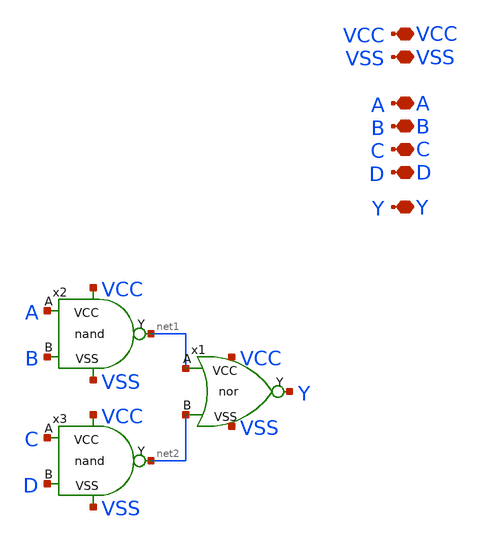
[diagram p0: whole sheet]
** sch_path: logic gates/and4.sch
**.subckt and4 VSS Y A B C VCC D
*.iopin VSS
*.iopin Y
*.iopin A
*.iopin B
*.iopin C
*.iopin VCC
*.iopin D
x1 VCC Y net1 net2 VSS nor
x2 VCC net1 A B VSS nand
x3 VCC net2 C D VSS nand
**.ends

* expanding   symbol:  logic gates/nor.sym # of pins=5
** sym_path: logic gates/nor.sym
** sch_path: logic gates/nor.sch
.subckt nor VCC Y A B VSS
*.iopin VCC
*.iopin VSS
*.iopin Y
*.iopin A
*.iopin B
XM2 Y B VSS VSS sky130_fd_pr__nfet_01v8 L=0.15 W=1 nf=1 ad='int((1 + 1)/2) * 1 / 1 * 0.29' as='int((1 + 2)/2) * 1 / 1 * 0.29'
+ pd='2*int((1 + 1)/2) * (1 / 1 + 0.29)' ps='2*int((1 + 2)/2) * (1 / 1 + 0.29)' nrd='0.29 / 1 ' nrs='0.29 / 1 '
+ sa=0 sb=0 sd=0 mult=1 m=1
XM11 Y B net1 VCC sky130_fd_pr__pfet_01v8 L=0.15 W=1 nf=1 ad='int((nf+1)/2) * W/nf * 0.29' as='int((nf+2)/2) * W/nf * 0.29'
+ pd='2*int((nf+1)/2) * (W/nf + 0.29)' ps='2*int((nf+2)/2) * (W/nf + 0.29)' nrd='0.29 / W' nrs='0.29 / W'
+ sa=0 sb=0 sd=0 mult=1 m=1
XM1 Y A VSS VSS sky130_fd_pr__nfet_01v8 L=0.15 W=1 nf=1 ad='int((1 + 1)/2) * 1 / 1 * 0.29' as='int((1 + 2)/2) * 1 / 1 * 0.29'
+ pd='2*int((1 + 1)/2) * (1 / 1 + 0.29)' ps='2*int((1 + 2)/2) * (1 / 1 + 0.29)' nrd='0.29 / 1 ' nrs='0.29 / 1 '
+ sa=0 sb=0 sd=0 mult=1 m=1
XM3 net1 A VCC VCC sky130_fd_pr__pfet_01v8 L=0.15 W=1 nf=1 ad='int((nf+1)/2) * W/nf * 0.29' as='int((nf+2)/2) * W/nf * 0.29'
+ pd='2*int((nf+1)/2) * (W/nf + 0.29)' ps='2*int((nf+2)/2) * (W/nf + 0.29)' nrd='0.29 / W' nrs='0.29 / W'
+ sa=0 sb=0 sd=0 mult=1 m=1
.ends


* expanding   symbol:  logic gates/nand.sym # of pins=5
** sym_path: logic gates/nand.sym
** sch_path: logic gates/nand.sch
.subckt nand VCC Y A B VSS
*.iopin VCC
*.iopin VSS
*.iopin Y
*.iopin A
*.iopin B
XM2 net1 B VSS VSS sky130_fd_pr__nfet_01v8 L=0.15 W=1 nf=1 ad='int((1 + 1)/2) * 1 / 1 * 0.29' as='int((1 + 2)/2) * 1 / 1 * 0.29'
+ pd='2*int((1 + 1)/2) * (1 / 1 + 0.29)' ps='2*int((1 + 2)/2) * (1 / 1 + 0.29)' nrd='0.29 / 1 ' nrs='0.29 / 1 '
+ sa=0 sb=0 sd=0 mult=1 m=1
XM11 Y A VCC VCC sky130_fd_pr__pfet_01v8 L=0.15 W=1 nf=1 ad='int((nf+1)/2) * W/nf * 0.29' as='int((nf+2)/2) * W/nf * 0.29'
+ pd='2*int((nf+1)/2) * (W/nf + 0.29)' ps='2*int((nf+2)/2) * (W/nf + 0.29)' nrd='0.29 / W' nrs='0.29 / W'
+ sa=0 sb=0 sd=0 mult=1 m=1
XM1 Y A net1 VSS sky130_fd_pr__nfet_01v8 L=0.15 W=1 nf=1 ad='int((1 + 1)/2) * 1 / 1 * 0.29' as='int((1 + 2)/2) * 1 / 1 * 0.29'
+ pd='2*int((1 + 1)/2) * (1 / 1 + 0.29)' ps='2*int((1 + 2)/2) * (1 / 1 + 0.29)' nrd='0.29 / 1 ' nrs='0.29 / 1 '
+ sa=0 sb=0 sd=0 mult=1 m=1
XM3 Y B VCC VCC sky130_fd_pr__pfet_01v8 L=0.15 W=1 nf=1 ad='int((nf+1)/2) * W/nf * 0.29' as='int((nf+2)/2) * W/nf * 0.29'
+ pd='2*int((nf+1)/2) * (W/nf + 0.29)' ps='2*int((nf+2)/2) * (W/nf + 0.29)' nrd='0.29 / W' nrs='0.29 / W'
+ sa=0 sb=0 sd=0 mult=1 m=1
.ends

.end
